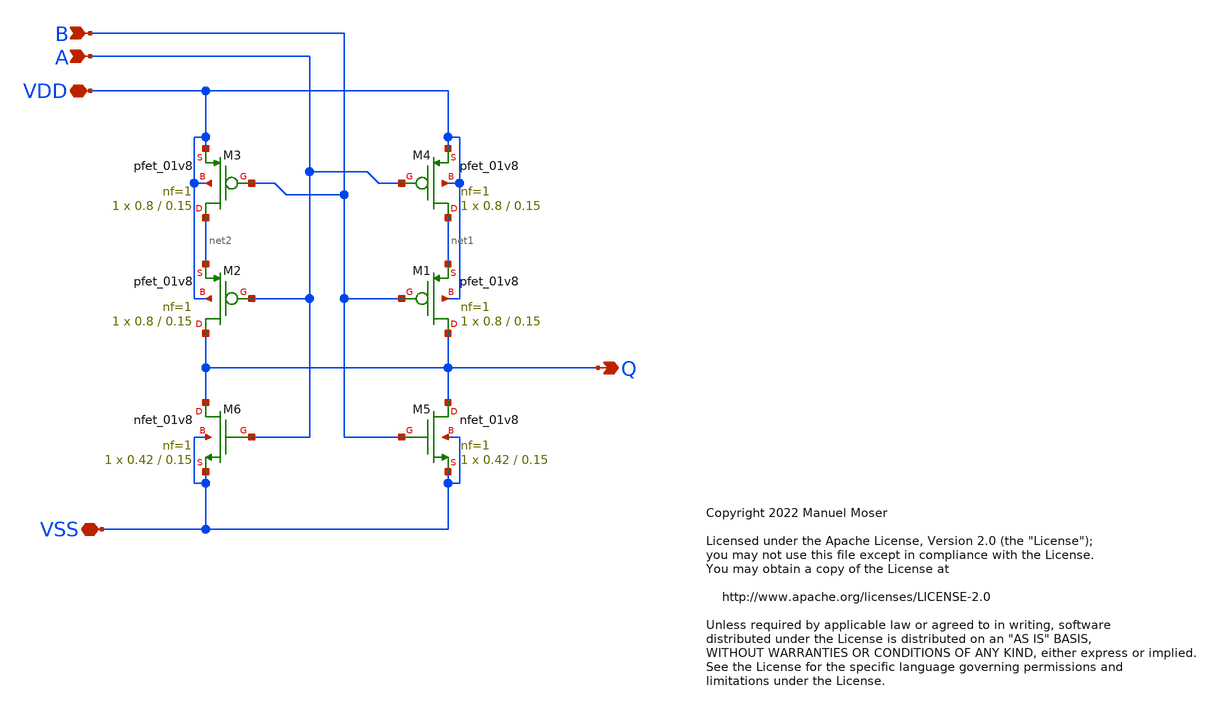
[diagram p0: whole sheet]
** sch_path: xschem/NOR/NOR_1.sch
* Copyright 2022 Manuel Moser
* Licensed under the Apache License, Version 2.0 (the "License");
**.subckt NOR_1 VDD VSS B A Q
*.iopin VDD
*.iopin VSS
*.ipin B
*.ipin A
*.opin Q
XM5 Q B VSS VSS sky130_fd_pr__nfet_01v8 L=0.15 W=0.42 nf=1 ad='int((nf+1)/2) * W/nf * 0.29' as='int((nf+2)/2) * W/nf * 0.29'
+ pd='2*int((nf+1)/2) * (W/nf + 0.29)' ps='2*int((nf+2)/2) * (W/nf + 0.29)' nrd='0.29 / W' nrs='0.29 / W'
+ sa=0 sb=0 sd=0 mult=1 m=1
XM6 Q A VSS VSS sky130_fd_pr__nfet_01v8 L=0.15 W=0.42 nf=1 ad='int((nf+1)/2) * W/nf * 0.29' as='int((nf+2)/2) * W/nf * 0.29'
+ pd='2*int((nf+1)/2) * (W/nf + 0.29)' ps='2*int((nf+2)/2) * (W/nf + 0.29)' nrd='0.29 / W' nrs='0.29 / W'
+ sa=0 sb=0 sd=0 mult=1 m=1
XM1 Q B net1 VDD sky130_fd_pr__pfet_01v8 L=0.15 W=0.8 nf=1 ad='int((nf+1)/2) * W/nf * 0.29' as='int((nf+2)/2) * W/nf * 0.29'
+ pd='2*int((nf+1)/2) * (W/nf + 0.29)' ps='2*int((nf+2)/2) * (W/nf + 0.29)' nrd='0.29 / W' nrs='0.29 / W'
+ sa=0 sb=0 sd=0 mult=1 m=1
XM2 Q A net2 VDD sky130_fd_pr__pfet_01v8 L=0.15 W=0.8 nf=1 ad='int((nf+1)/2) * W/nf * 0.29' as='int((nf+2)/2) * W/nf * 0.29'
+ pd='2*int((nf+1)/2) * (W/nf + 0.29)' ps='2*int((nf+2)/2) * (W/nf + 0.29)' nrd='0.29 / W' nrs='0.29 / W'
+ sa=0 sb=0 sd=0 mult=1 m=1
XM3 net2 B VDD VDD sky130_fd_pr__pfet_01v8 L=0.15 W=0.8 nf=1 ad='int((nf+1)/2) * W/nf * 0.29' as='int((nf+2)/2) * W/nf * 0.29'
+ pd='2*int((nf+1)/2) * (W/nf + 0.29)' ps='2*int((nf+2)/2) * (W/nf + 0.29)' nrd='0.29 / W' nrs='0.29 / W'
+ sa=0 sb=0 sd=0 mult=1 m=1
XM4 net1 A VDD VDD sky130_fd_pr__pfet_01v8 L=0.15 W=0.8 nf=1 ad='int((nf+1)/2) * W/nf * 0.29' as='int((nf+2)/2) * W/nf * 0.29'
+ pd='2*int((nf+1)/2) * (W/nf + 0.29)' ps='2*int((nf+2)/2) * (W/nf + 0.29)' nrd='0.29 / W' nrs='0.29 / W'
+ sa=0 sb=0 sd=0 mult=1 m=1
**.ends
.end
